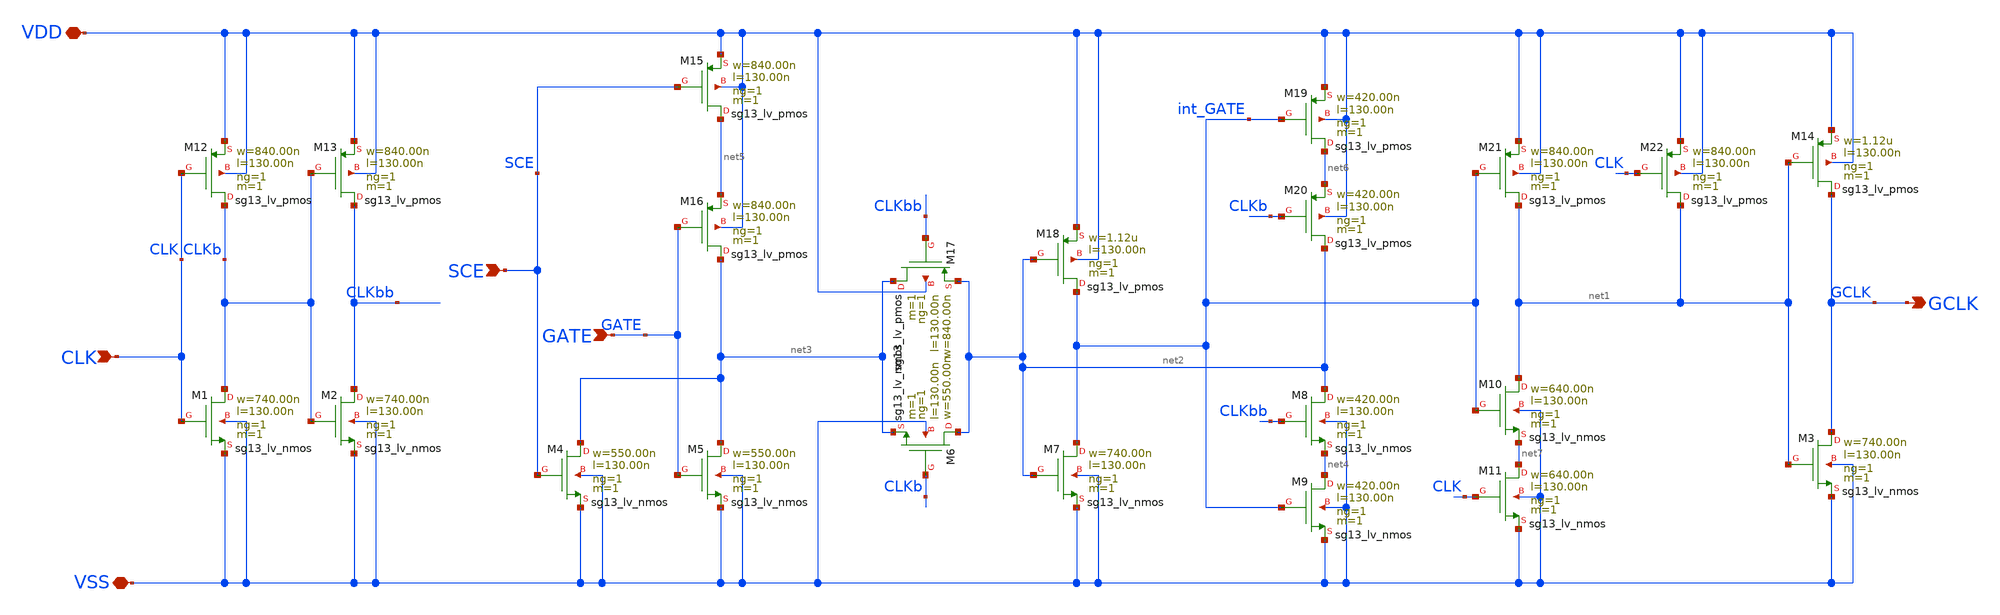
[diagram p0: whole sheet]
** sch_path: ihp-sg13g2/libs.tech/xschem/sg13g2_stdcells/sg13g2_slgcp_1.sch
* Copyright 2023 IHP PDK Authors
* Licensed under the Apache License, Version 2.0 (the "License");
* you may not use this file except in compliance with the License.
* You may obtain a copy of the License at
* https://www.apache.org/licenses/LICENSE-2.0
* Unless required by applicable law or agreed to in writing, software
* distributed under the License is distributed on an "AS IS" BASIS,
* WITHOUT WARRANTIES OR CONDITIONS OF ANY KIND, either express or implied.
* See the License for the specific language governing permissions and
* limitations under the License.
**.subckt sg13g2_slgcp_1 GCLK SCE GATE CLK VDD VSS
*.opin GCLK
*.ipin SCE
*.ipin GATE
*.ipin CLK
*.iopin VDD
*.iopin VSS
XM1 CLKb CLK VSS VSS sg13_lv_nmos w=740.00n l=130.00n ng=1 m=1 mm_ok=1
XM2 CLKbb CLKb VSS VSS sg13_lv_nmos w=740.00n l=130.00n ng=1 m=1 mm_ok=1
XM3 GCLK net1 VSS VSS sg13_lv_nmos w=740.00n l=130.00n ng=1 m=1 mm_ok=1
XM4 net3 SCE VSS VSS sg13_lv_nmos w=550.00n l=130.00n ng=1 m=1 mm_ok=1
XM5 net3 GATE VSS VSS sg13_lv_nmos w=550.00n l=130.00n ng=1 m=1 mm_ok=1
XM6 net2 CLKb net3 VSS sg13_lv_nmos w=550.00n l=130.00n ng=1 m=1 mm_ok=1
XM7 int_GATE net2 VSS VSS sg13_lv_nmos w=740.00n l=130.00n ng=1 m=1 mm_ok=1
XM8 net2 CLKbb net4 VSS sg13_lv_nmos w=420.00n l=130.00n ng=1 m=1 mm_ok=1
XM9 net4 int_GATE VSS VSS sg13_lv_nmos w=420.00n l=130.00n ng=1 m=1 mm_ok=1
XM10 net1 int_GATE net7 VSS sg13_lv_nmos w=640.00n l=130.00n ng=1 m=1 mm_ok=1
XM11 net7 CLK VSS VSS sg13_lv_nmos w=640.00n l=130.00n ng=1 m=1 mm_ok=1
XM12 CLKb CLK VDD VDD sg13_lv_pmos w=840.00n l=130.00n ng=1 m=1 mm_ok=1
XM13 CLKbb CLKb VDD VDD sg13_lv_pmos w=840.00n l=130.00n ng=1 m=1 mm_ok=1
XM14 GCLK net1 VDD VDD sg13_lv_pmos w=1.12u l=130.00n ng=1 m=1 mm_ok=1
XM15 net5 SCE VDD VDD sg13_lv_pmos w=840.00n l=130.00n ng=1 m=1 mm_ok=1
XM16 net3 GATE net5 VDD sg13_lv_pmos w=840.00n l=130.00n ng=1 m=1 mm_ok=1
XM17 net3 CLKbb net2 VDD sg13_lv_pmos w=840.00n l=130.00n ng=1 m=1 mm_ok=1
XM18 int_GATE net2 VDD VDD sg13_lv_pmos w=1.12u l=130.00n ng=1 m=1 mm_ok=1
XM19 net6 int_GATE VDD VDD sg13_lv_pmos w=420.00n l=130.00n ng=1 m=1 mm_ok=1
XM20 net2 CLKb net6 VDD sg13_lv_pmos w=420.00n l=130.00n ng=1 m=1 mm_ok=1
XM21 net1 int_GATE VDD VDD sg13_lv_pmos w=840.00n l=130.00n ng=1 m=1 mm_ok=1
XM22 net1 CLK VDD VDD sg13_lv_pmos w=840.00n l=130.00n ng=1 m=1 mm_ok=1
**.ends
.end
